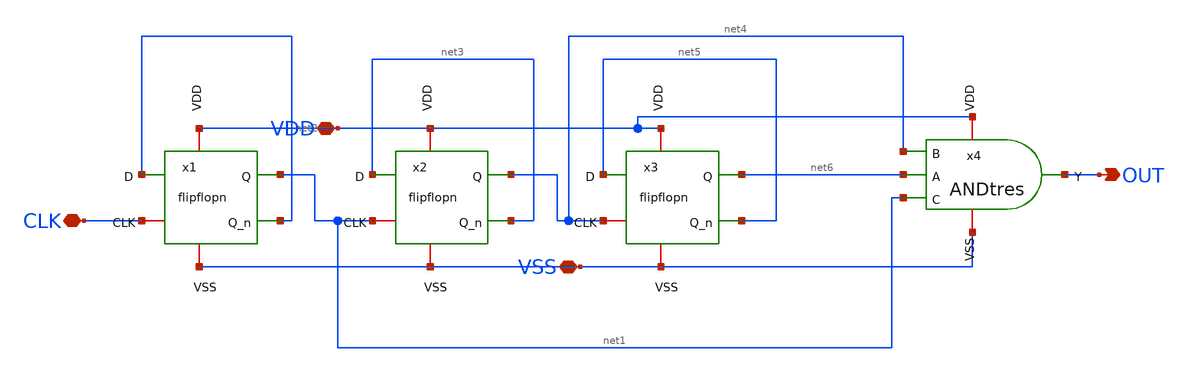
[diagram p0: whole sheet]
** sch_path: netlist/cont.sch
**.subckt cont OUT CLK VDD VSS
*.opin OUT
*.iopin CLK
*.iopin VDD
*.iopin VSS
x1 CLK net2 VDD net1 net2 VSS flipflopn
x2 net1 net3 VDD net4 net3 VSS flipflopn
x3 net4 net5 VDD net6 net5 VSS flipflopn
x4 VDD net4 net6 OUT net1 VSS ANDtres
**.ends
.end
